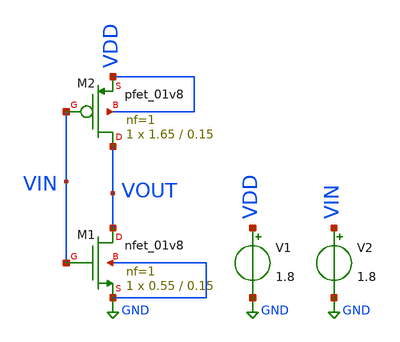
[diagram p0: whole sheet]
** sch_path: xschem/inverter.sch
**.subckt inverter
XM1 VOUT VIN GND GND sky130_fd_pr__nfet_01v8 L=0.15 W=0.55 nf=1 ad='int((nf+1)/2) * W/nf * 0.29' as='int((nf+2)/2) * W/nf * 0.29'
+ pd='2*int((nf+1)/2) * (W/nf + 0.29)' ps='2*int((nf+2)/2) * (W/nf + 0.29)' nrd='0.29 / W' nrs='0.29 / W'
+ sa=0 sb=0 sd=0 mult=1 m=1
XM2 VOUT VIN VDD VDD sky130_fd_pr__pfet_01v8 L=0.15 W=1.65 nf=1 ad='int((nf+1)/2) * W/nf * 0.29' as='int((nf+2)/2) * W/nf * 0.29'
+ pd='2*int((nf+1)/2) * (W/nf + 0.29)' ps='2*int((nf+2)/2) * (W/nf + 0.29)' nrd='0.29 / W' nrs='0.29 / W'
+ sa=0 sb=0 sd=0 mult=1 m=1
V1 VDD GND 1.8
V2 VIN GND 1.8
**** begin user architecture code


.option wnflag=0
.option savecurrents
.control
dc V2 0 1.8 0.01
plot V(VIN) V(VOUT)
.endc

 .lib $::SKYWATER_MODELS/sky130.lib.spice tt
.include $::SKYWATER_STDCELLS/../../sky130_fd_sc_hvl/spice/sky130_fd_sc_hvl.spice

.param mc_mm_switch=0
.param mc_pr_switch=1

**** end user architecture code
**.ends
.GLOBAL GND
.end
